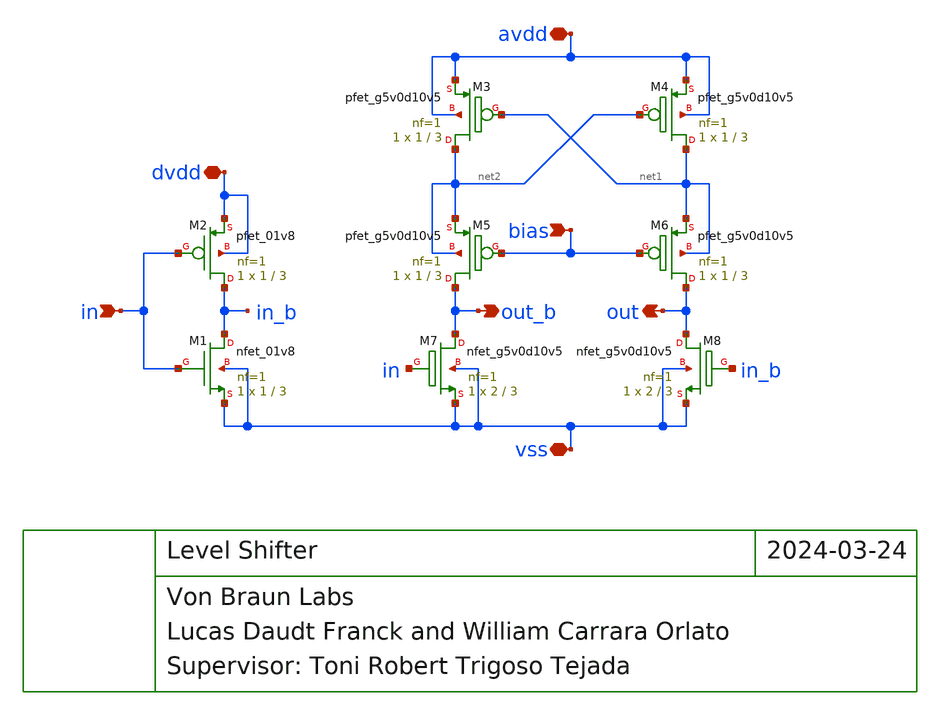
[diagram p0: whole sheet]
** sch_path: blocks/input/xschem/level_shifter.sch
**.subckt level_shifter avdd out_b out vss dvdd in bias
*.iopin avdd
*.opin out_b
*.opin out
*.iopin vss
*.iopin dvdd
*.ipin in
*.ipin bias
XM1 in_b in vss vss sky130_fd_pr__nfet_01v8 L=3 W=1 nf=1 ad='int((nf+1)/2) * W/nf * 0.29' as='int((nf+2)/2) * W/nf * 0.29'
+ pd='2*int((nf+1)/2) * (W/nf + 0.29)' ps='2*int((nf+2)/2) * (W/nf + 0.29)' nrd='0.29 / W' nrs='0.29 / W'
+ sa=0 sb=0 sd=0 mult=1 m=1
XM2 in_b in dvdd dvdd sky130_fd_pr__pfet_01v8 L=3 W=1 nf=1 ad='int((nf+1)/2) * W/nf * 0.29' as='int((nf+2)/2) * W/nf * 0.29'
+ pd='2*int((nf+1)/2) * (W/nf + 0.29)' ps='2*int((nf+2)/2) * (W/nf + 0.29)' nrd='0.29 / W' nrs='0.29 / W'
+ sa=0 sb=0 sd=0 mult=1 m=1
XM3 net2 net1 avdd avdd sky130_fd_pr__pfet_g5v0d10v5 L=3 W=1 nf=1 ad='int((nf+1)/2) * W/nf * 0.29' as='int((nf+2)/2) * W/nf * 0.29'
+ pd='2*int((nf+1)/2) * (W/nf + 0.29)' ps='2*int((nf+2)/2) * (W/nf + 0.29)' nrd='0.29 / W' nrs='0.29 / W'
+ sa=0 sb=0 sd=0 mult=1 m=1
XM4 net1 net2 avdd avdd sky130_fd_pr__pfet_g5v0d10v5 L=3 W=1 nf=1 ad='int((nf+1)/2) * W/nf * 0.29' as='int((nf+2)/2) * W/nf * 0.29'
+ pd='2*int((nf+1)/2) * (W/nf + 0.29)' ps='2*int((nf+2)/2) * (W/nf + 0.29)' nrd='0.29 / W' nrs='0.29 / W'
+ sa=0 sb=0 sd=0 mult=1 m=1
XM5 out_b bias net2 net2 sky130_fd_pr__pfet_g5v0d10v5 L=3 W=1 nf=1 ad='int((nf+1)/2) * W/nf * 0.29' as='int((nf+2)/2) * W/nf * 0.29'
+ pd='2*int((nf+1)/2) * (W/nf + 0.29)' ps='2*int((nf+2)/2) * (W/nf + 0.29)' nrd='0.29 / W' nrs='0.29 / W'
+ sa=0 sb=0 sd=0 mult=1 m=1
XM6 out bias net1 net1 sky130_fd_pr__pfet_g5v0d10v5 L=3 W=1 nf=1 ad='int((nf+1)/2) * W/nf * 0.29' as='int((nf+2)/2) * W/nf * 0.29'
+ pd='2*int((nf+1)/2) * (W/nf + 0.29)' ps='2*int((nf+2)/2) * (W/nf + 0.29)' nrd='0.29 / W' nrs='0.29 / W'
+ sa=0 sb=0 sd=0 mult=1 m=1
XM8 out in_b vss vss sky130_fd_pr__nfet_g5v0d10v5 L=3 W=2 nf=1 ad='int((nf+1)/2) * W/nf * 0.29' as='int((nf+2)/2) * W/nf * 0.29'
+ pd='2*int((nf+1)/2) * (W/nf + 0.29)' ps='2*int((nf+2)/2) * (W/nf + 0.29)' nrd='0.29 / W' nrs='0.29 / W'
+ sa=0 sb=0 sd=0 mult=1 m=1
XM7 out_b in vss vss sky130_fd_pr__nfet_g5v0d10v5 L=3 W=2 nf=1 ad='int((nf+1)/2) * W/nf * 0.29' as='int((nf+2)/2) * W/nf * 0.29'
+ pd='2*int((nf+1)/2) * (W/nf + 0.29)' ps='2*int((nf+2)/2) * (W/nf + 0.29)' nrd='0.29 / W' nrs='0.29 / W'
+ sa=0 sb=0 sd=0 mult=1 m=1
**.ends
.end
